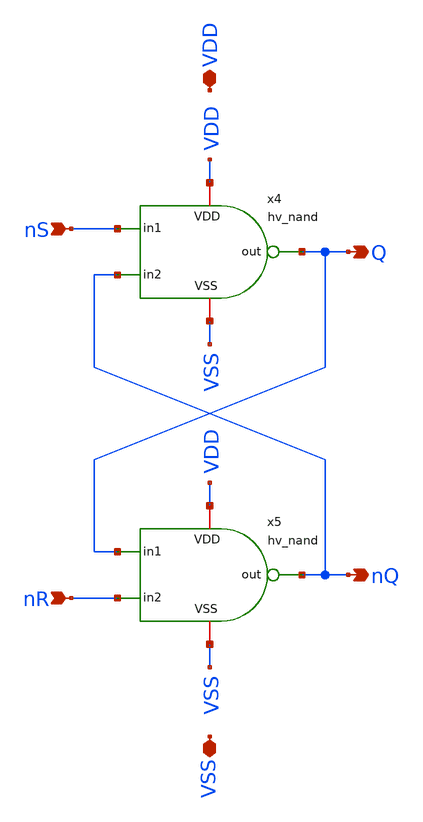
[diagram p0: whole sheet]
** sch_path: macros/heichips26_vcr/macros/switched_capacitor/schematic/xschem/hv_rs-ff.sch
**.subckt hv_rs-ff nS VDD VSS Q nR nQ
*.ipin nS
*.iopin VDD
*.iopin VSS
*.opin Q
*.ipin nR
*.opin nQ
x4 VDD nS Q nQ VSS hv_nand
x5 VDD Q nQ nR VSS hv_nand
**.ends

* expanding   symbol:  hv_nand.sym # of pins=5
** sym_path: macros/heichips26_vcr/macros/switched_capacitor/schematic/xschem/hv_nand.sym
** sch_path: macros/heichips26_vcr/macros/switched_capacitor/schematic/xschem/hv_nand.sch
.subckt hv_nand VDD in1 out in2 VSS
*.ipin in1
*.iopin VDD
*.iopin VSS
*.opin out
*.ipin in2
**** begin user architecture code


.param w   = 10u
.param ng  = 4
.param n_ng = ng
.param n_w = {3u*n_ng}
.param n_l = 0.45u
.param p_ng = ng
.param p_w = {10u*p_ng}
.param p_l = 0.4u


**** end user architecture code
XM2 out in1 net1 VSS sg13_hv_nmos w={n_w} l={n_l} ng={ng} m=1 mm_ok=1
XM3 out in2 VDD VDD sg13_hv_pmos w={p_w} l={p_l} ng={ng} m=1 mm_ok=1
XM1 net1 in2 VSS VSS sg13_hv_nmos w={n_w} l={n_l} ng={ng} m=1 mm_ok=1
XM4 out in1 VDD VDD sg13_hv_pmos w={p_w} l={p_l} ng={ng} m=1 mm_ok=1
.ends

.end
